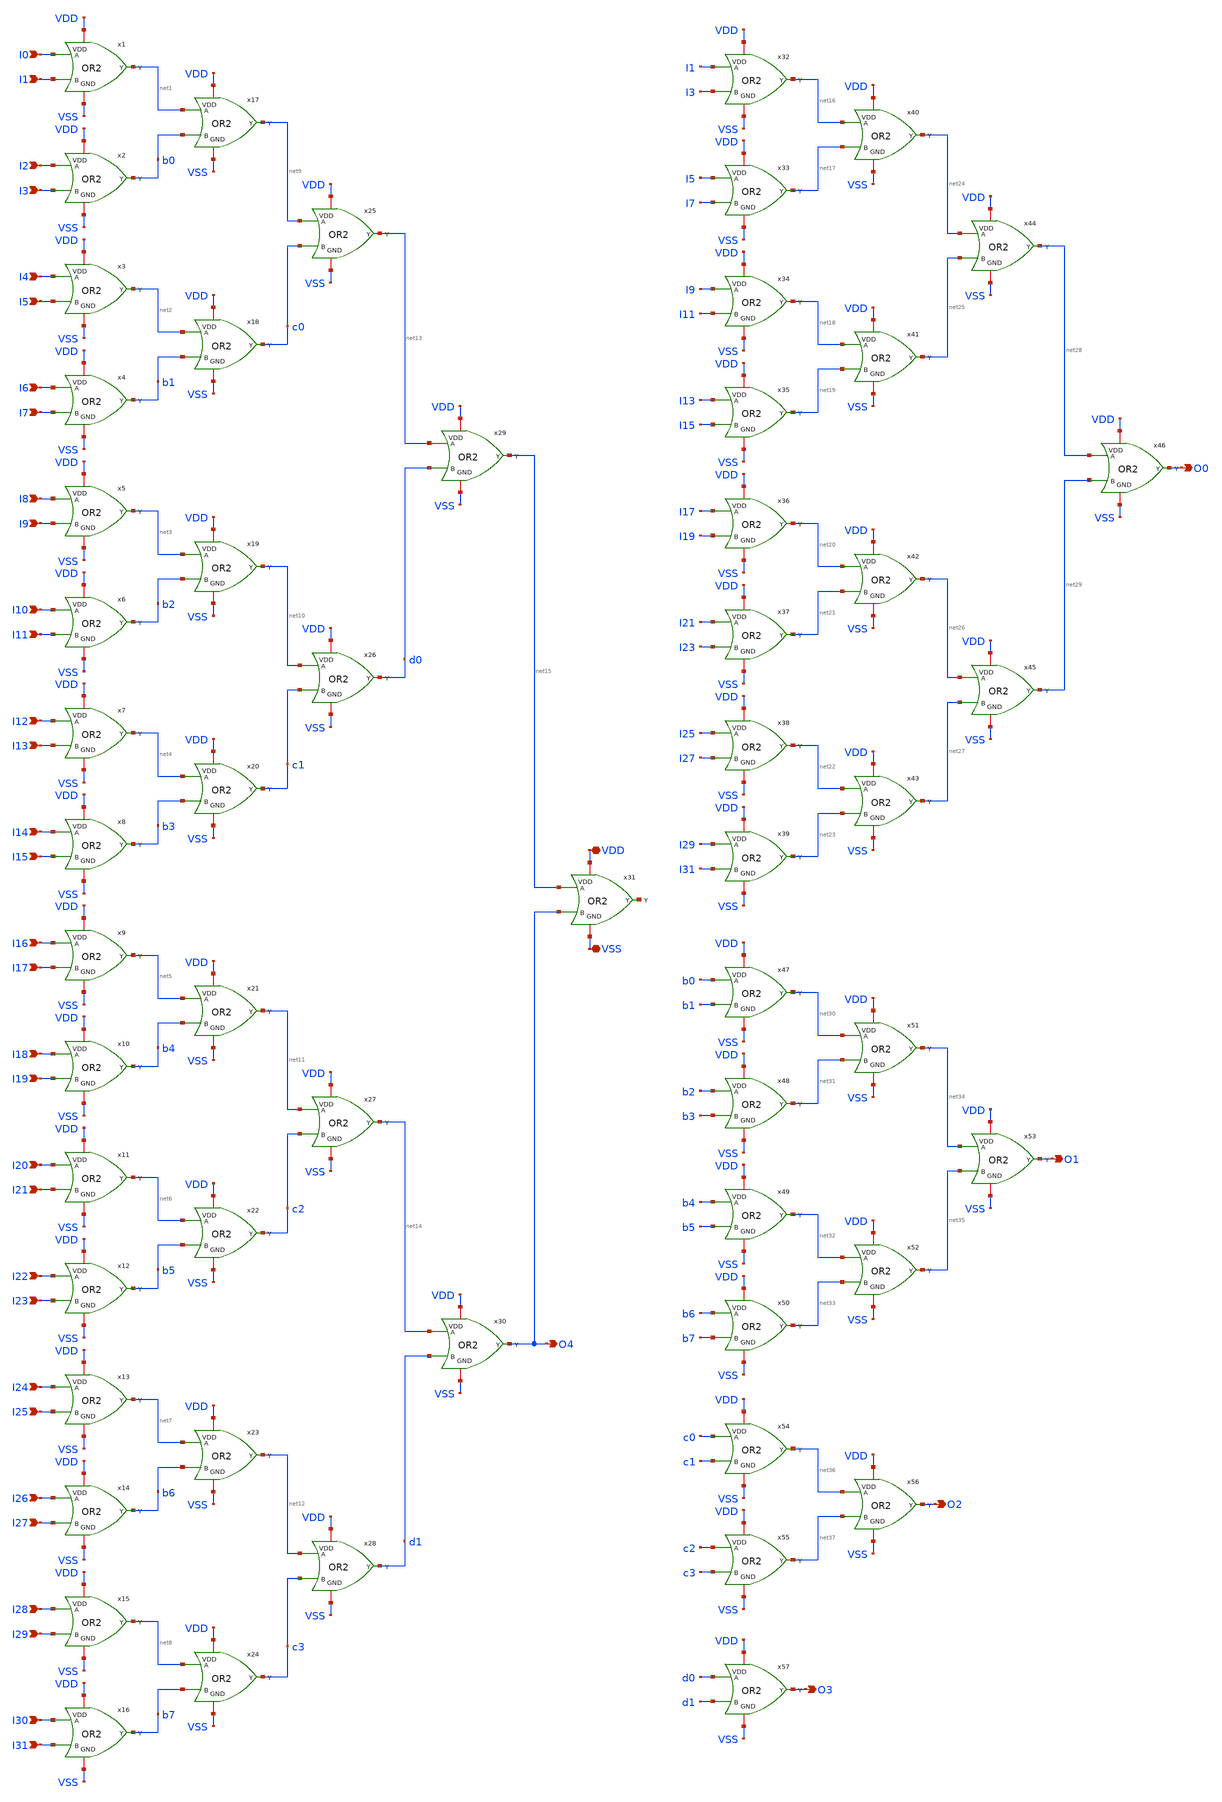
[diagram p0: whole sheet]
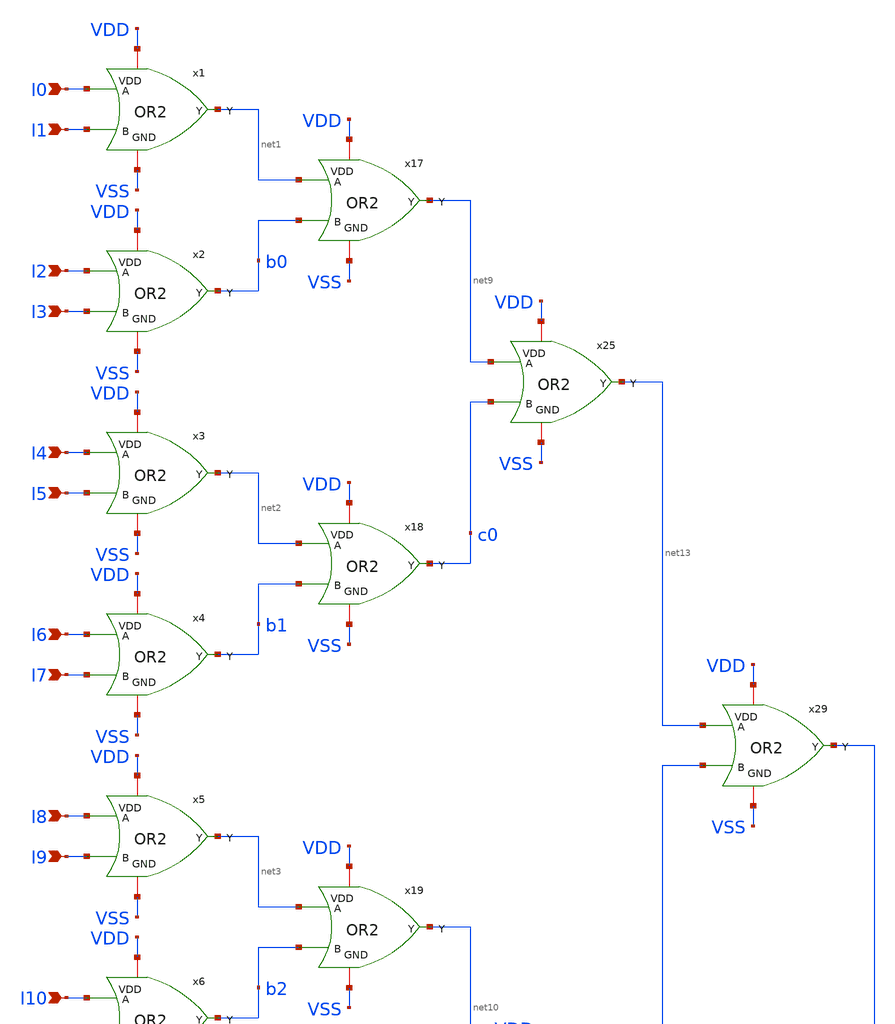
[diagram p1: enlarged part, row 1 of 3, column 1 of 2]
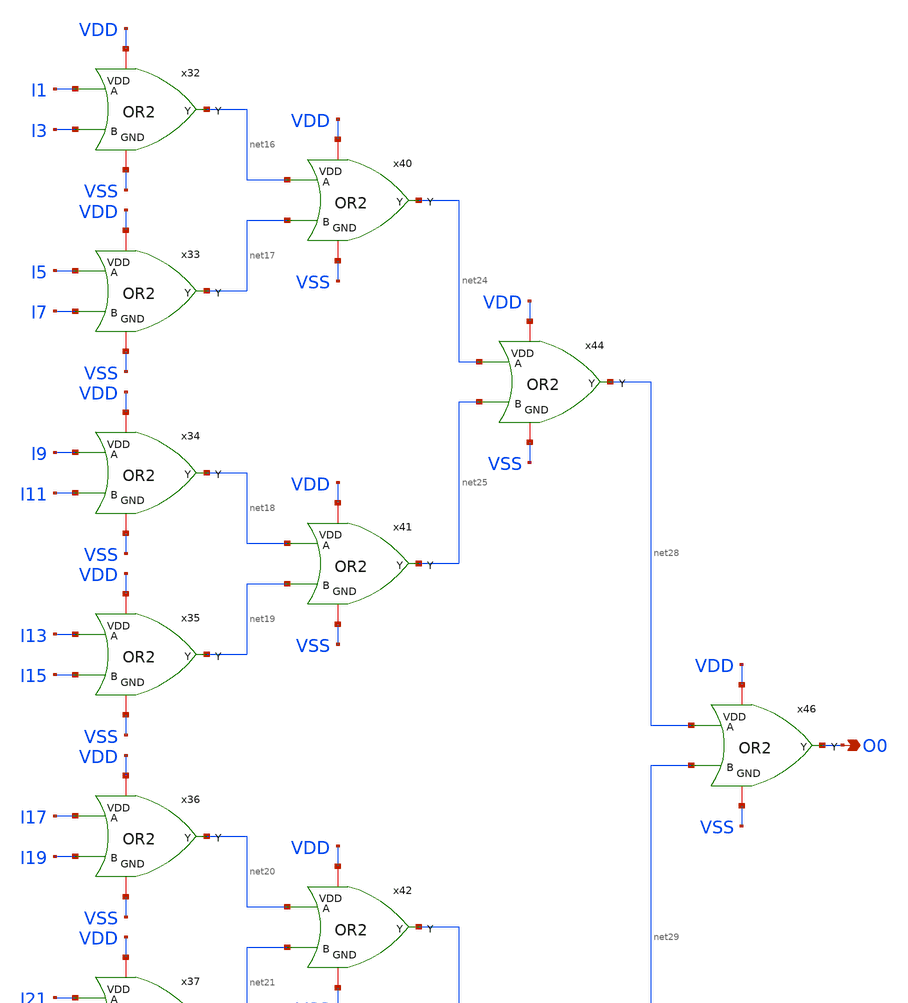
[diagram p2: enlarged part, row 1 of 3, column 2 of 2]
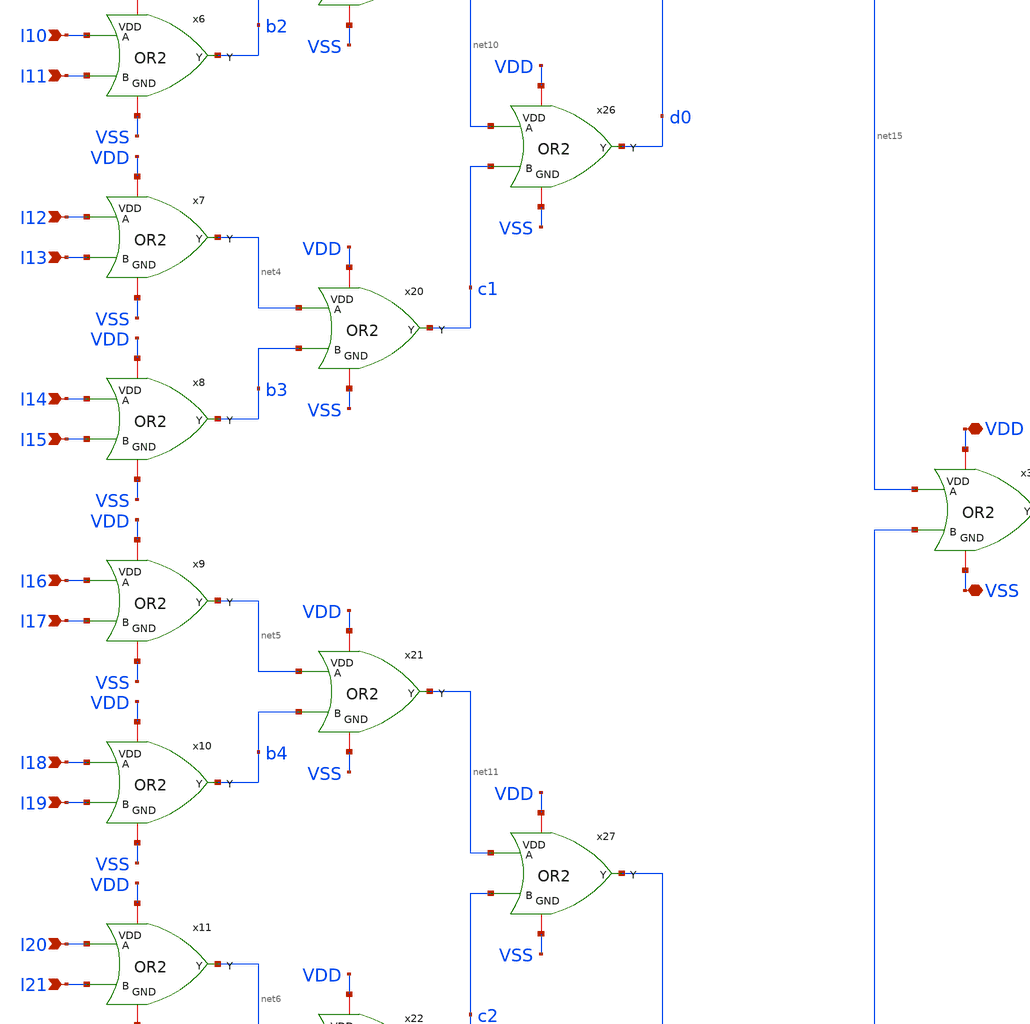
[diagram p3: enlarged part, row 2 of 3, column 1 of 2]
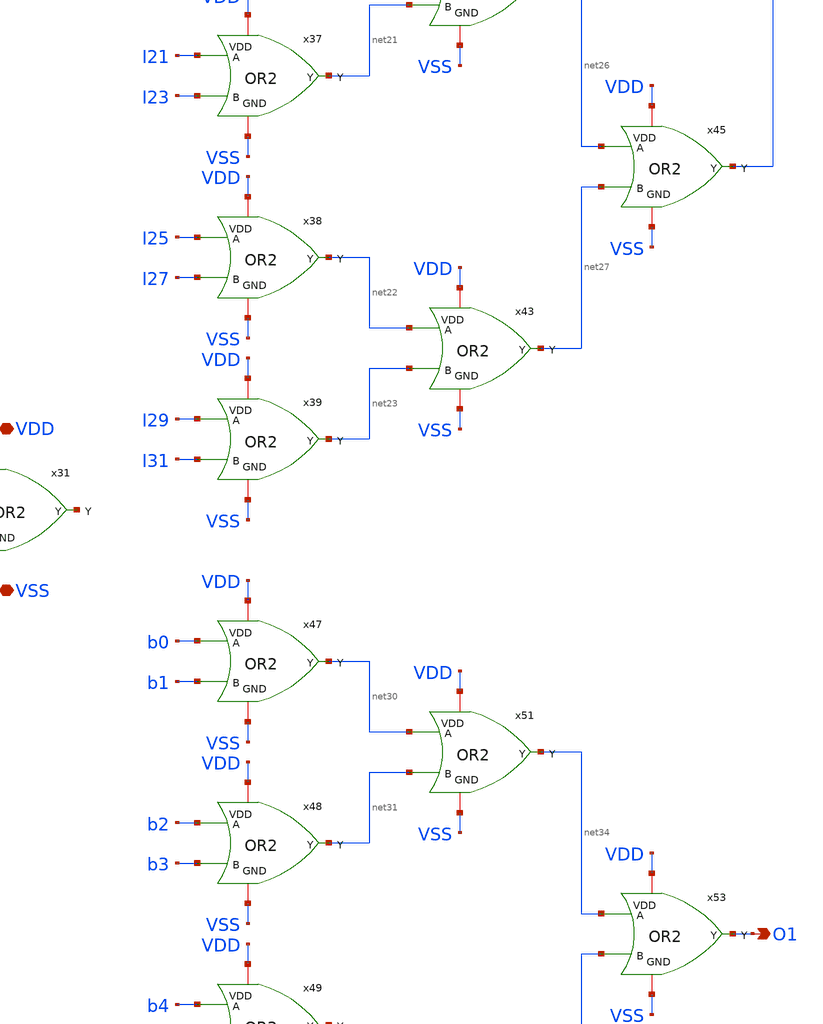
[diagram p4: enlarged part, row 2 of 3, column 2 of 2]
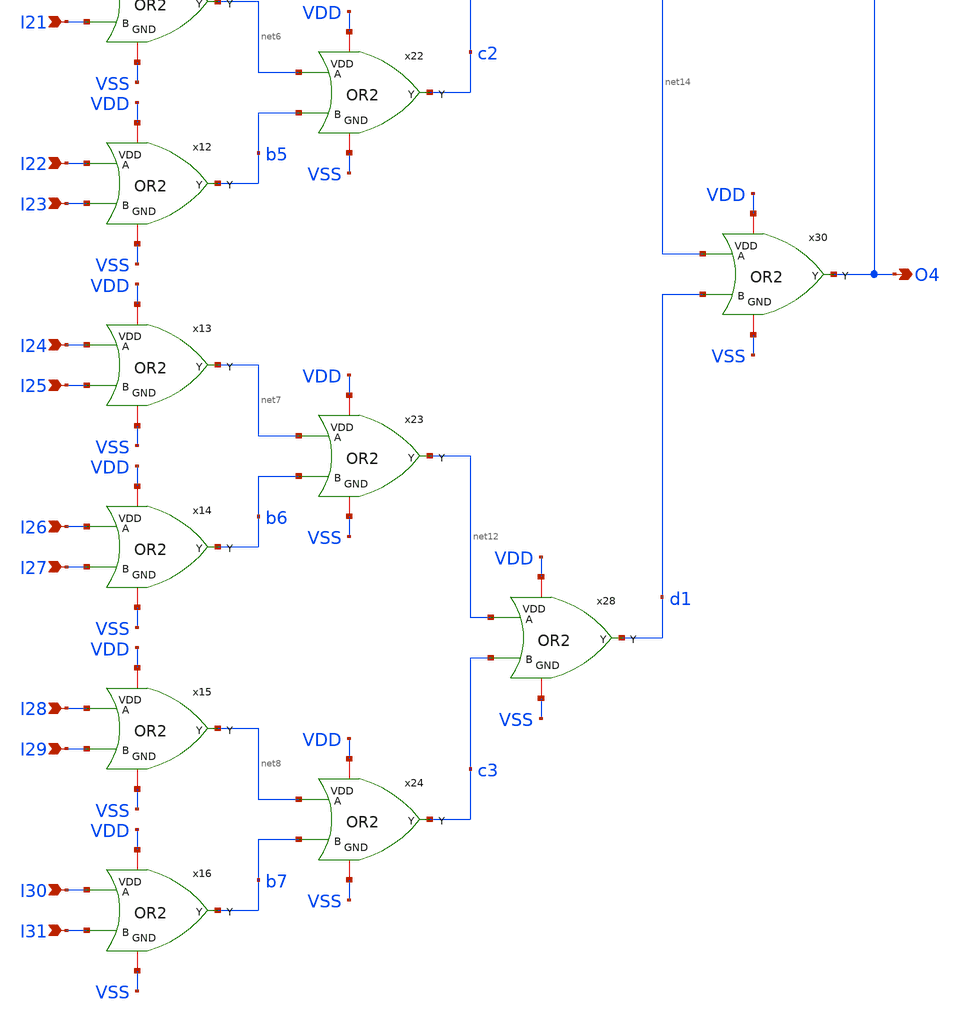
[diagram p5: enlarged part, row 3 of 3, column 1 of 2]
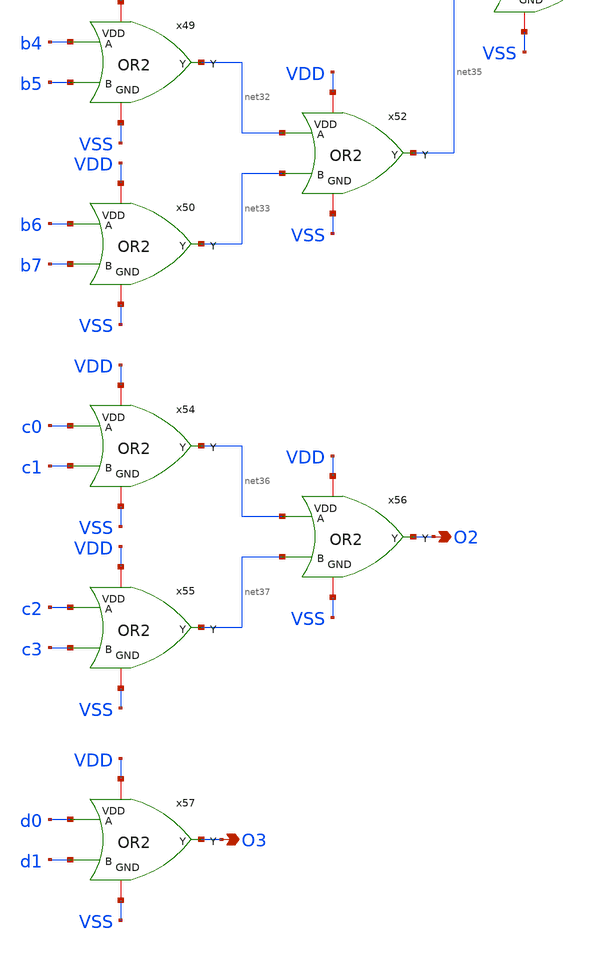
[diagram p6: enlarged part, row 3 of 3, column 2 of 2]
** sch_path: Vol.2/files/04/xschem/Fat_tree_encoder.sch
**.subckt Fat_tree_encoder I0 I1 I2 I3 I4 I5 I6 I7 I8 I9 I10 I11 I12 I13 I14 I15 I16 I17 I18 I19 I20
*+ I21 I22 I23 I24 I25 I26 I27 I28 I29 I30 I31 O4 O0 O1 O2 O3 VDD VSS
*.ipin I0
*.ipin I1
*.ipin I2
*.ipin I3
*.ipin I4
*.ipin I5
*.ipin I6
*.ipin I7
*.ipin I8
*.ipin I9
*.ipin I10
*.ipin I11
*.ipin I12
*.ipin I13
*.ipin I14
*.ipin I15
*.ipin I16
*.ipin I17
*.ipin I18
*.ipin I19
*.ipin I20
*.ipin I21
*.ipin I22
*.ipin I23
*.ipin I24
*.ipin I25
*.ipin I26
*.ipin I27
*.ipin I28
*.ipin I29
*.ipin I30
*.ipin I31
*.opin O4
*.opin O0
*.opin O1
*.opin O2
*.opin O3
*.iopin VDD
*.iopin VSS
x1 VDD net1 I0 I1 VSS OR2
x2 VDD b0 I2 I3 VSS OR2
x3 VDD net2 I4 I5 VSS OR2
x4 VDD b1 I6 I7 VSS OR2
x5 VDD net3 I8 I9 VSS OR2
x6 VDD b2 I10 I11 VSS OR2
x7 VDD net4 I12 I13 VSS OR2
x8 VDD b3 I14 I15 VSS OR2
x9 VDD net5 I16 I17 VSS OR2
x10 VDD b4 I18 I19 VSS OR2
x11 VDD net6 I20 I21 VSS OR2
x12 VDD b5 I22 I23 VSS OR2
x13 VDD net7 I24 I25 VSS OR2
x14 VDD b6 I26 I27 VSS OR2
x15 VDD net8 I28 I29 VSS OR2
x16 VDD b7 I30 I31 VSS OR2
x17 VDD net9 net1 b0 VSS OR2
x18 VDD c0 net2 b1 VSS OR2
x19 VDD net10 net3 b2 VSS OR2
x20 VDD c1 net4 b3 VSS OR2
x21 VDD net11 net5 b4 VSS OR2
x22 VDD c2 net6 b5 VSS OR2
x23 VDD net12 net7 b6 VSS OR2
x24 VDD c3 net8 b7 VSS OR2
x25 VDD net13 net9 c0 VSS OR2
x26 VDD d0 net10 c1 VSS OR2
x27 VDD net14 net11 c2 VSS OR2
x28 VDD d1 net12 c3 VSS OR2
x29 VDD net15 net13 d0 VSS OR2
x30 VDD O4 net14 d1 VSS OR2
x31 VDD net38 net15 O4 VSS OR2
x32 VDD net16 I1 I3 VSS OR2
x33 VDD net17 I5 I7 VSS OR2
x34 VDD net18 I9 I11 VSS OR2
x35 VDD net19 I13 I15 VSS OR2
x36 VDD net20 I17 I19 VSS OR2
x37 VDD net21 I21 I23 VSS OR2
x38 VDD net22 I25 I27 VSS OR2
x39 VDD net23 I29 I31 VSS OR2
x40 VDD net24 net16 net17 VSS OR2
x41 VDD net25 net18 net19 VSS OR2
x42 VDD net26 net20 net21 VSS OR2
x43 VDD net27 net22 net23 VSS OR2
x44 VDD net28 net24 net25 VSS OR2
x45 VDD net29 net26 net27 VSS OR2
x46 VDD O0 net28 net29 VSS OR2
x47 VDD net30 b0 b1 VSS OR2
x48 VDD net31 b2 b3 VSS OR2
x49 VDD net32 b4 b5 VSS OR2
x50 VDD net33 b6 b7 VSS OR2
x51 VDD net34 net30 net31 VSS OR2
x52 VDD net35 net32 net33 VSS OR2
x53 VDD O1 net34 net35 VSS OR2
x54 VDD net36 c0 c1 VSS OR2
x55 VDD net37 c2 c3 VSS OR2
x56 VDD O2 net36 net37 VSS OR2
x57 VDD O3 d0 d1 VSS OR2
**.ends

* expanding   symbol:  IP62_5_stdcell/OR2.sym # of pins=5
** sym_path: IP62_5_stdcell/OR2.sym
** sch_path: IP62_5_stdcell/OR2.sch
.subckt OR2 VDD Y A B GND
*.ipin A
*.ipin B
*.opin Y
*.iopin VDD
*.iopin GND
XM7 net2 B VDD VDD PMOS w=10.2u l=1u as=0 ad=0 ps=0 pd=0 nrd=0 nrs=0 m=1
XM2 net1 A net2 VDD PMOS w=10.2u l=1u as=0 ad=0 ps=0 pd=0 nrd=0 nrs=0 m=1
XM4 Y net1 VDD VDD PMOS w=10.2u l=1u as=0 ad=0 ps=0 pd=0 nrd=0 nrs=0 m=1
XM1 net1 B GND GND NMOS w=3.4u l=1u as=0 ad=0 ps=0 pd=0 nrd=0 nrs=0 m=1
XM3 net1 A GND GND NMOS w=3.4u l=1u as=0 ad=0 ps=0 pd=0 nrd=0 nrs=0 m=1
XM5 Y net1 GND GND NMOS w=3.4u l=1u as=0 ad=0 ps=0 pd=0 nrd=0 nrs=0 m=1
.ends

.end
